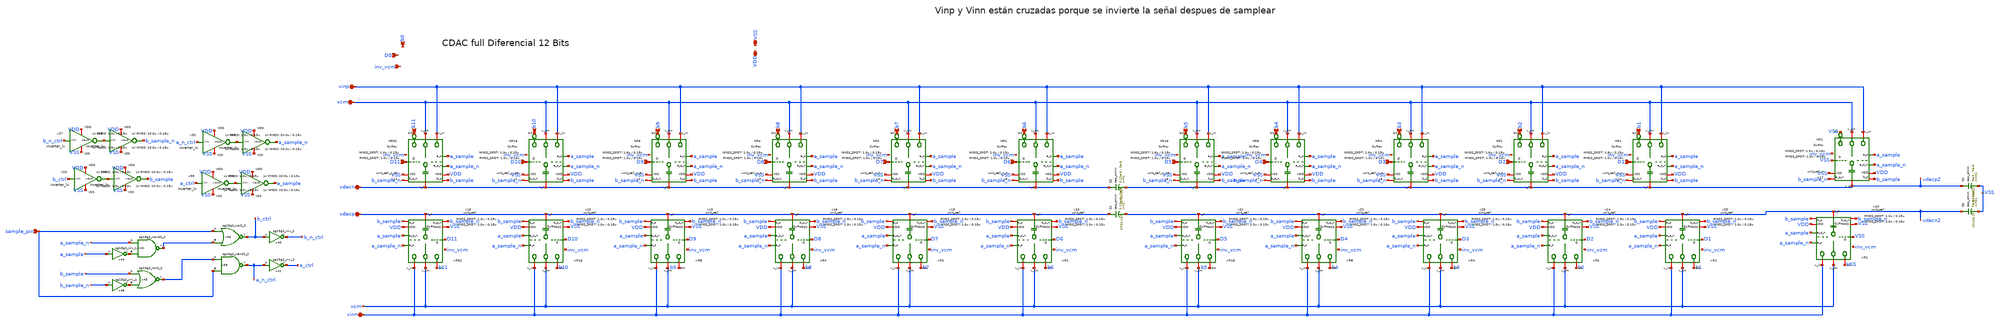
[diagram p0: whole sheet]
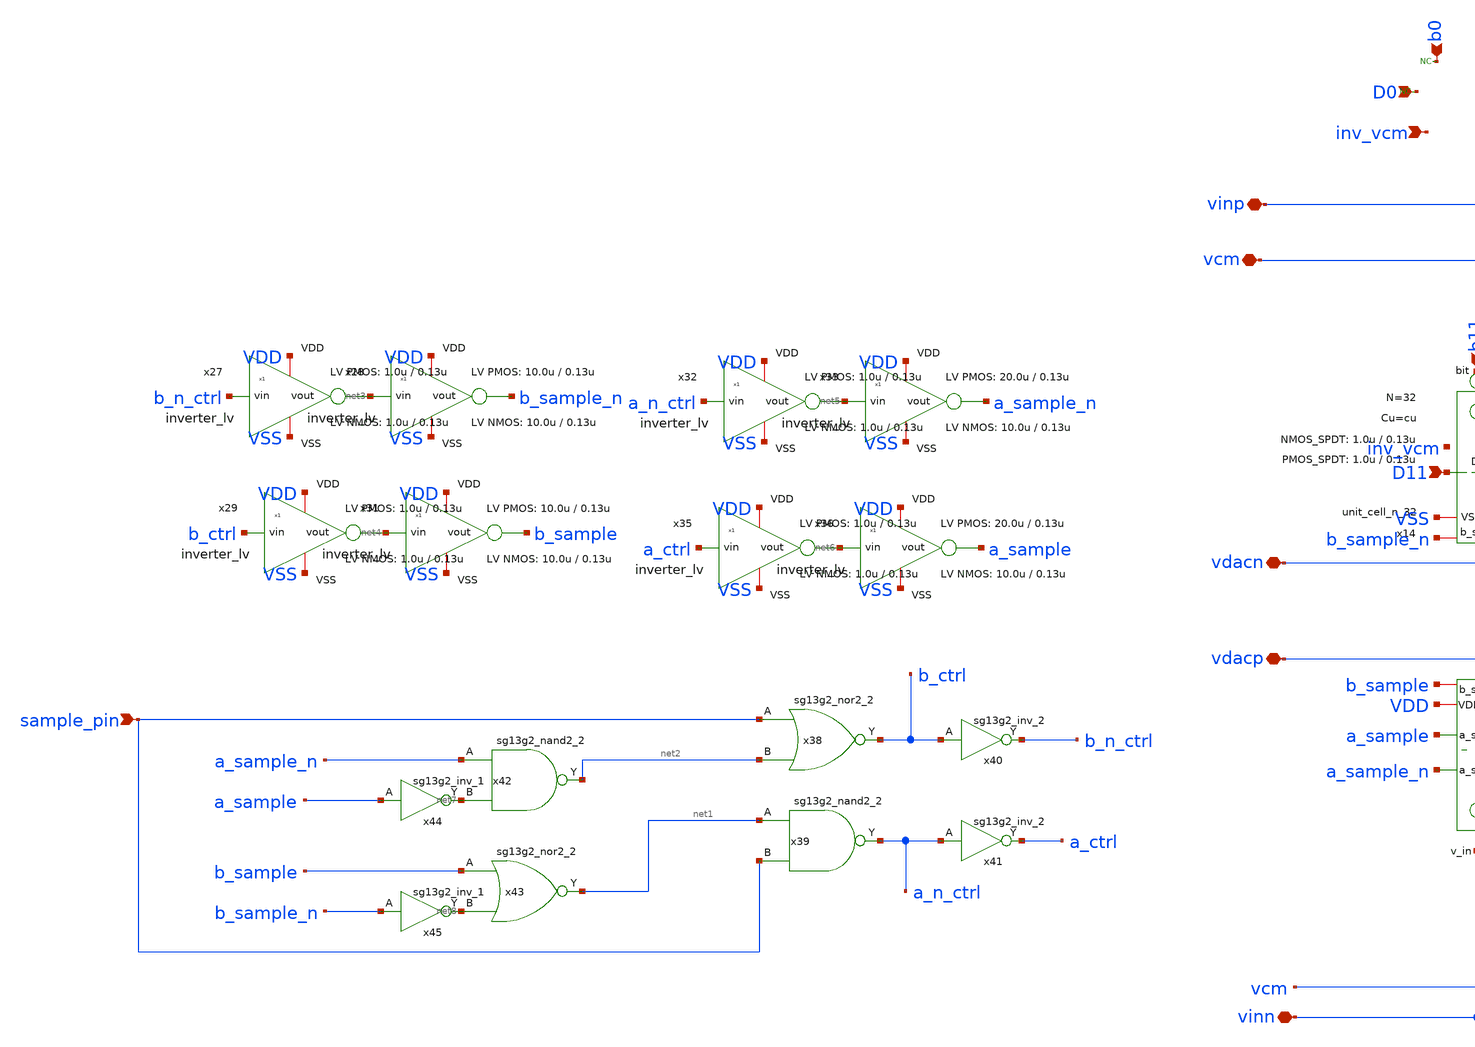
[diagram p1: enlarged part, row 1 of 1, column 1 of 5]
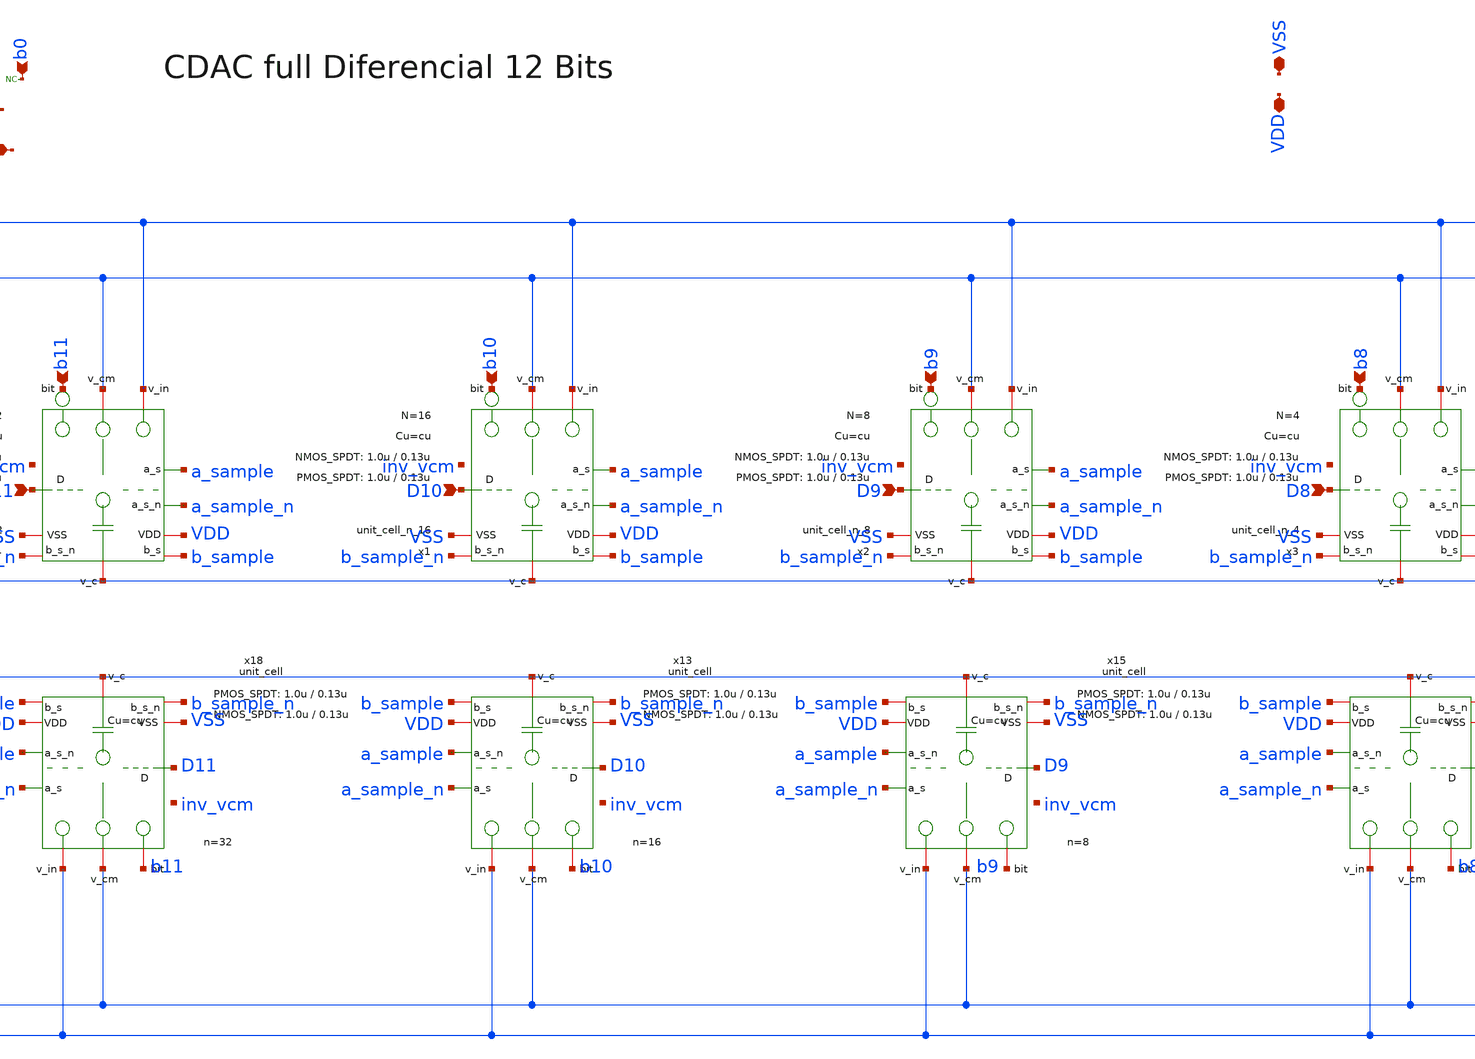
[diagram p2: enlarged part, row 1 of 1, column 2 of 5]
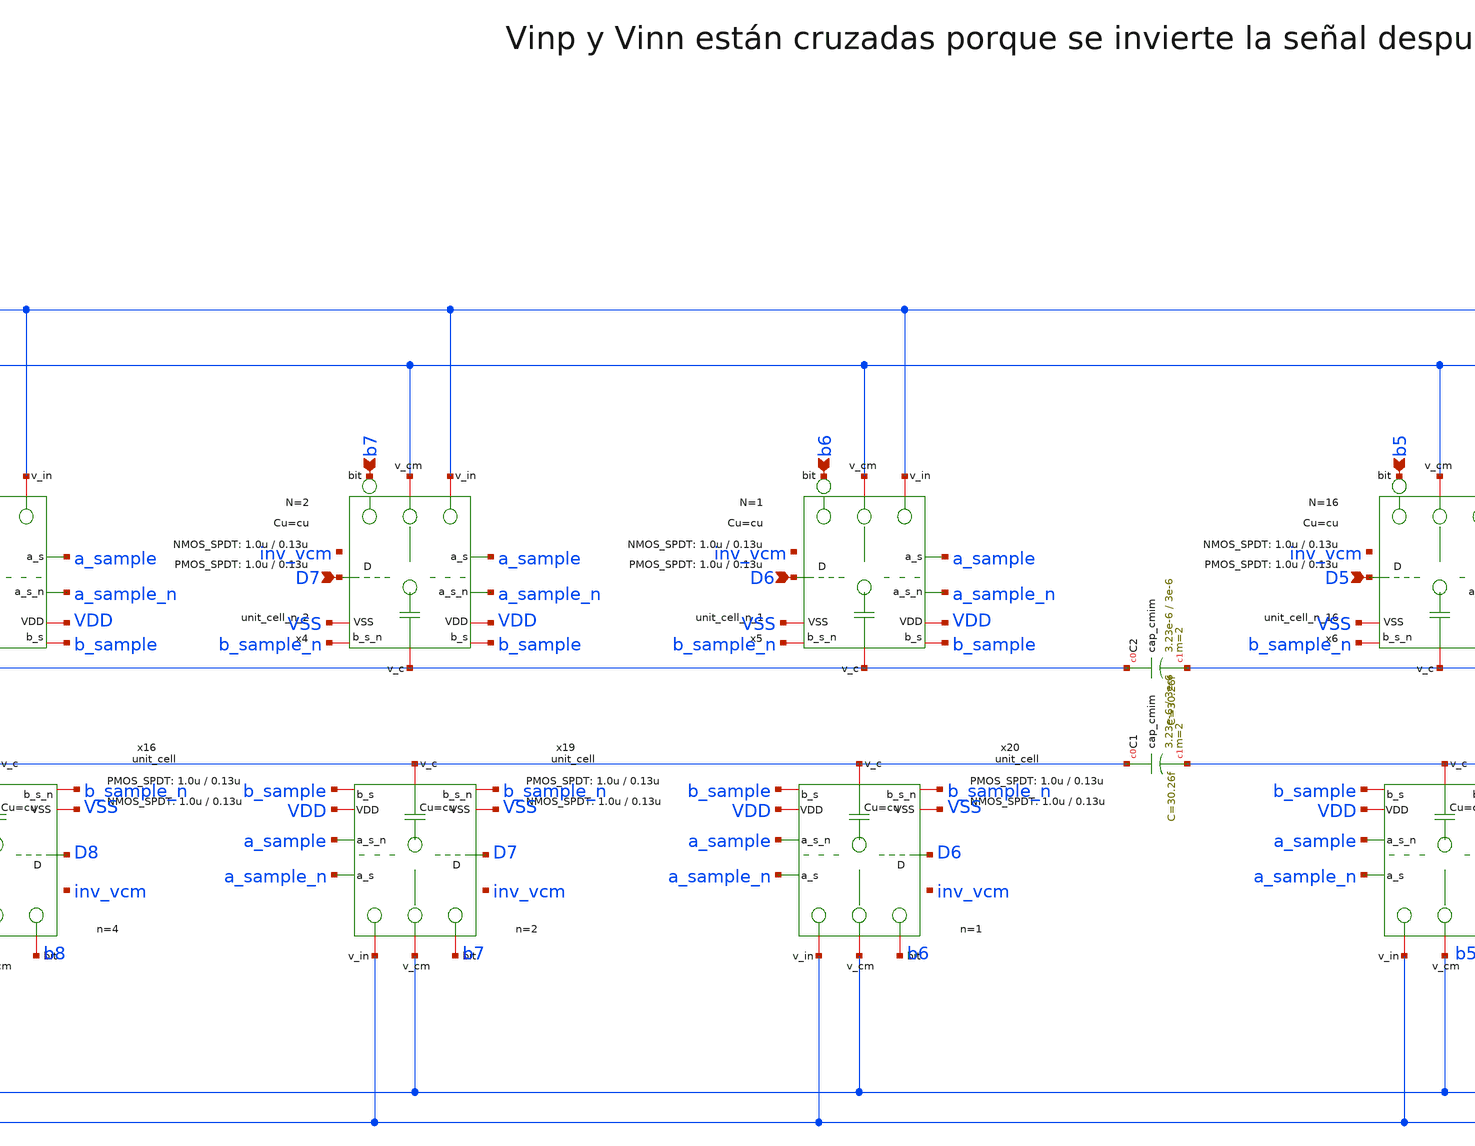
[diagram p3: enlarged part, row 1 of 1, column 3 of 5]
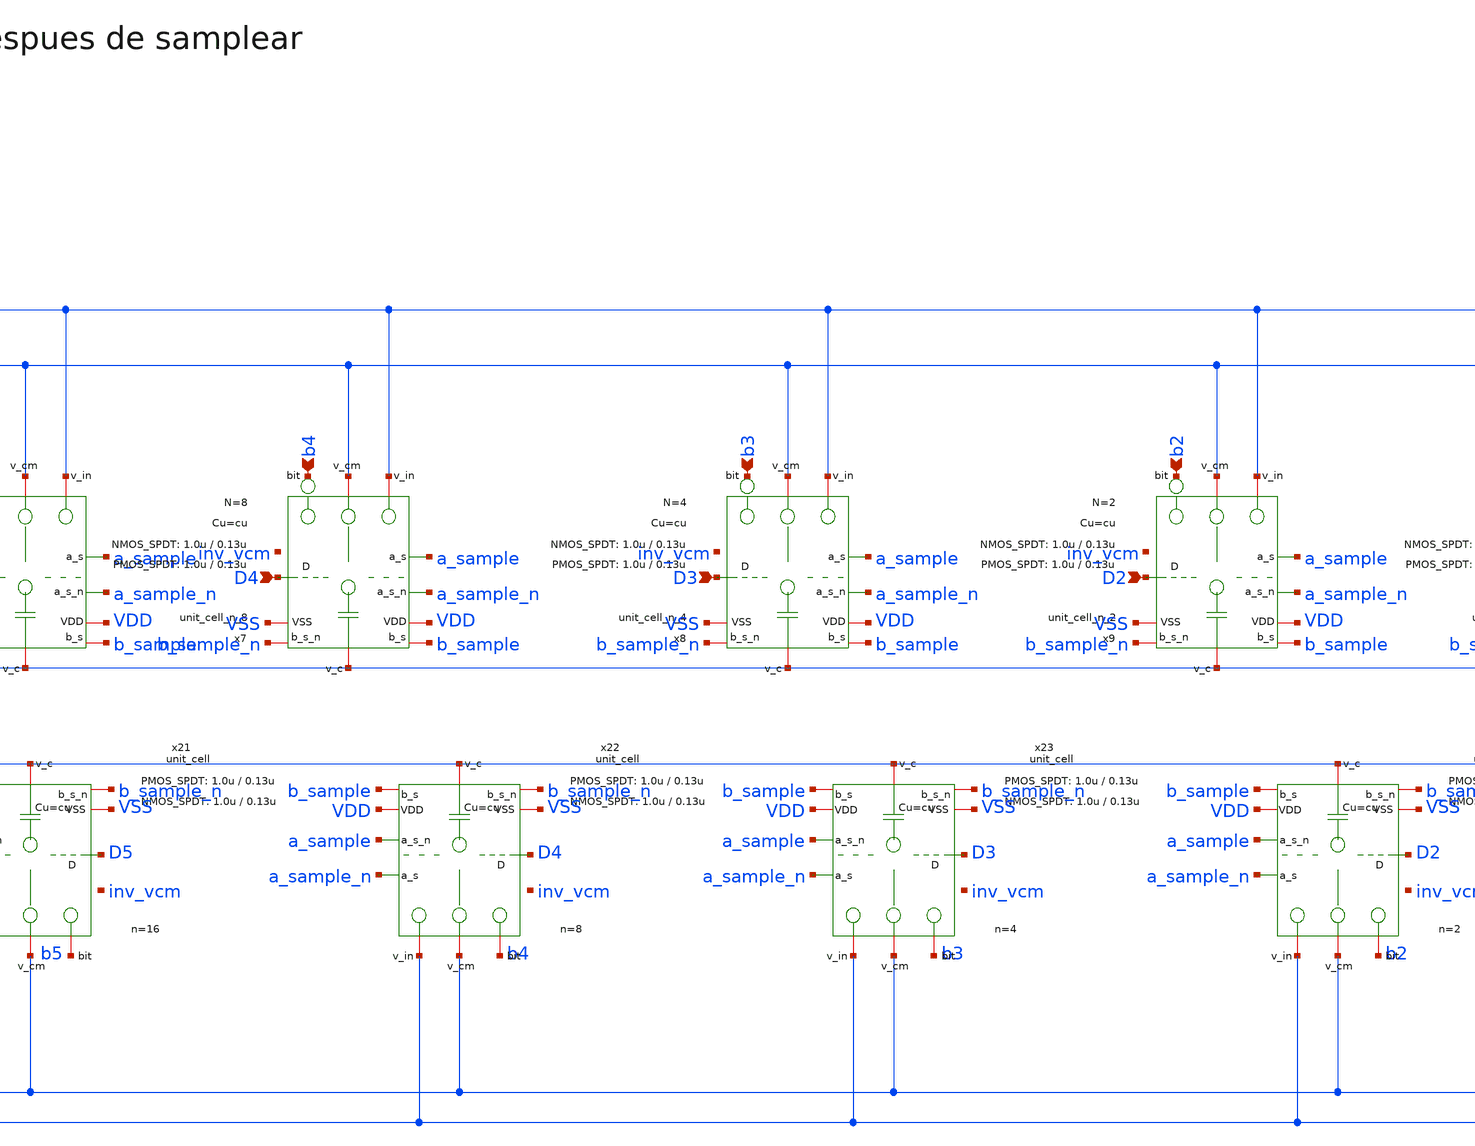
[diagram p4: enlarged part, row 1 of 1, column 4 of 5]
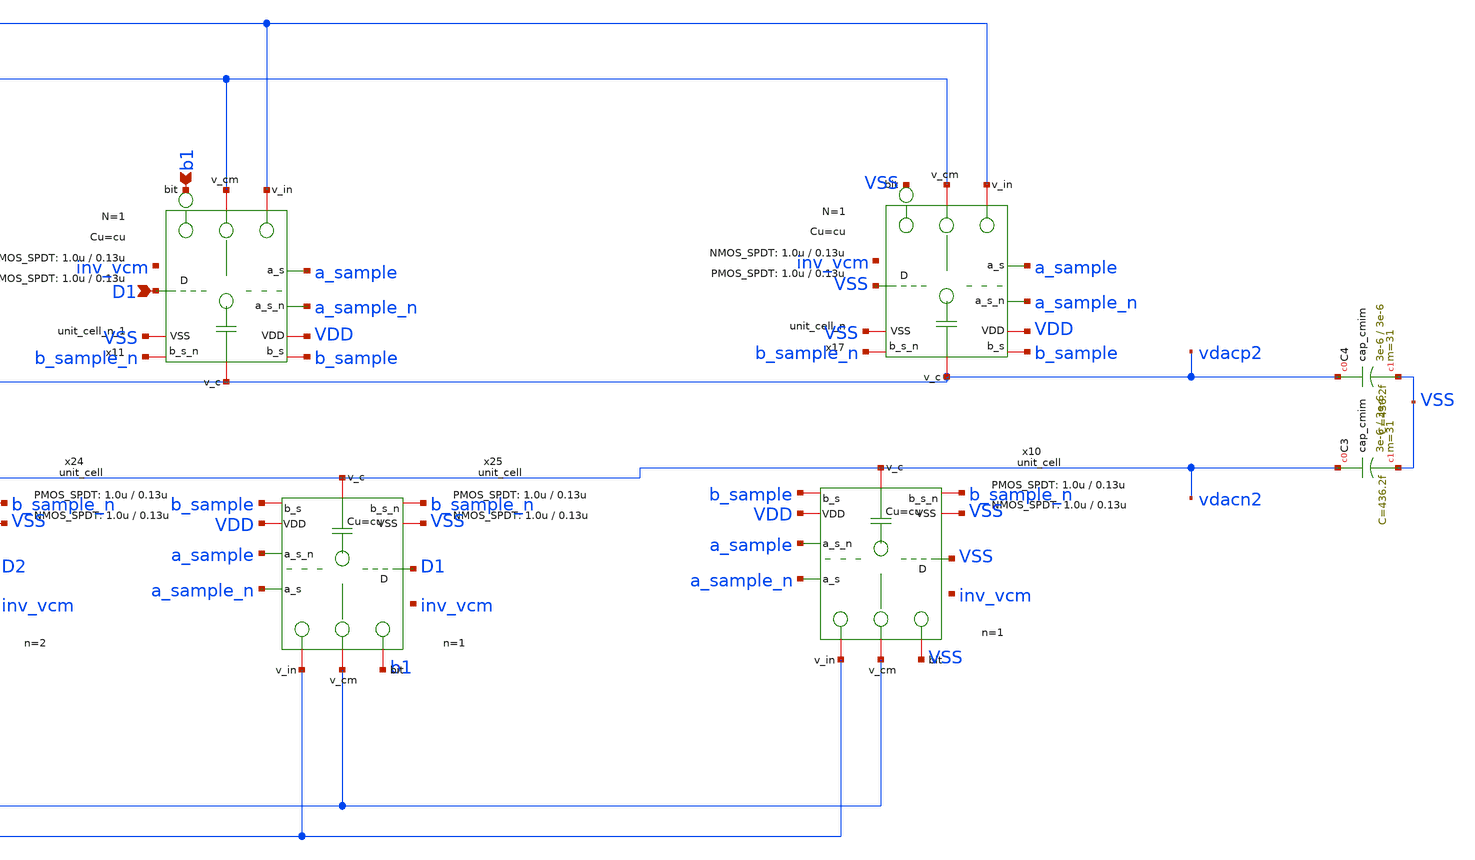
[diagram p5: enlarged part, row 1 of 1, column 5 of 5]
** sch_path: xschem/dac_icms_cell/dac.sch
**.subckt dac D0 b0 vinn vcm sample_pin vinp vdacp vdacn VSS VDD D1 b1 D2 b2 D3 b3 D4 b4 D5 b5 b6 D7
*+ b7 D8 b8 D9 b9 D10 b10 D11 b11 D6 inv_vcm
*.ipin D0
*.ipin b0
*.iopin vinn
*.iopin vcm
*.ipin sample_pin
*.iopin vinp
*.iopin vdacp
*.iopin vdacn
*.iopin VSS
*.iopin VDD
*.ipin D1
*.ipin b1
*.ipin D2
*.ipin b2
*.ipin D3
*.ipin b3
*.ipin D4
*.ipin b4
*.ipin D5
*.ipin b5
*.ipin b6
*.ipin D7
*.ipin b7
*.ipin D8
*.ipin b8
*.ipin D9
*.ipin b9
*.ipin D10
*.ipin b10
*.ipin D11
*.ipin b11
*.ipin D6
*.ipin inv_vcm
x14 VDD D11 VSS vdacn b11 vcm vinp a_sample a_sample_n b_sample b_sample_n inv_vcm unit_cell_n_32
x18 VDD D11 VSS vdacp b11 vcm vinn a_sample_n a_sample b_sample b_sample_n inv_vcm unit_cell W_P=
+ L_P_SPDT=0.13u W_N= L_N_SPDT=0.13u Cu=cu n=32
x1 VDD D10 VSS vdacn b10 vcm vinp a_sample a_sample_n b_sample b_sample_n inv_vcm unit_cell_n_16
x2 VDD D9 VSS vdacn b9 vcm vinp a_sample a_sample_n b_sample b_sample_n inv_vcm unit_cell_n_8
x3 VDD D8 VSS vdacn b8 vcm vinp a_sample a_sample_n b_sample b_sample_n inv_vcm unit_cell_n_4
x4 VDD D7 VSS vdacn b7 vcm vinp a_sample a_sample_n b_sample b_sample_n inv_vcm unit_cell_n_2
x5 VDD D6 VSS vdacn b6 vcm vinp a_sample a_sample_n b_sample b_sample_n inv_vcm unit_cell_n_1
x6 VDD D5 VSS vdacp2 b5 vcm vinp a_sample a_sample_n b_sample b_sample_n inv_vcm unit_cell_n_16
x7 VDD D4 VSS vdacp2 b4 vcm vinp a_sample a_sample_n b_sample b_sample_n inv_vcm unit_cell_n_8
x8 VDD D3 VSS vdacp2 b3 vcm vinp a_sample a_sample_n b_sample b_sample_n inv_vcm unit_cell_n_4
x9 VDD D2 VSS vdacp2 b2 vcm vinp a_sample a_sample_n b_sample b_sample_n inv_vcm unit_cell_n_2
x11 VDD D1 VSS vdacp2 b1 vcm vinp a_sample a_sample_n b_sample b_sample_n inv_vcm unit_cell_n_1
x13 VDD D10 VSS vdacp b10 vcm vinn a_sample_n a_sample b_sample b_sample_n inv_vcm unit_cell W_P=
+ L_P_SPDT=0.13u W_N= L_N_SPDT=0.13u Cu=cu n=16
x15 VDD D9 VSS vdacp b9 vcm vinn a_sample_n a_sample b_sample b_sample_n inv_vcm unit_cell W_P=
+ L_P_SPDT=0.13u W_N= L_N_SPDT=0.13u Cu=cu n=8
x16 VDD D8 VSS vdacp b8 vcm vinn a_sample_n a_sample b_sample b_sample_n inv_vcm unit_cell W_P=
+ L_P_SPDT=0.13u W_N= L_N_SPDT=0.13u Cu=cu n=4
x19 VDD D7 VSS vdacp b7 vcm vinn a_sample_n a_sample b_sample b_sample_n inv_vcm unit_cell W_P=1.0u
+ L_P_SPDT=0.13u W_N=1.0u L_N_SPDT=0.13u Cu=cu n=2
x20 VDD D6 VSS vdacp b6 vcm vinn a_sample_n a_sample b_sample b_sample_n inv_vcm unit_cell W_P=
+ L_P_SPDT=0.13u W_N= L_N_SPDT=0.13u Cu=cu n=1
x21 VDD D5 VSS vdacn2 b5 vcm vinn a_sample_n a_sample b_sample b_sample_n inv_vcm unit_cell W_P=
+ L_P_SPDT=0.13u W_N= L_N_SPDT=0.13u Cu=cu n=16
x22 VDD D4 VSS vdacn2 b4 vcm vinn a_sample_n a_sample b_sample b_sample_n inv_vcm unit_cell W_P=
+ L_P_SPDT=0.13u W_N= L_N_SPDT=0.13u Cu=cu n=8
x23 VDD D3 VSS vdacn2 b3 vcm vinn a_sample_n a_sample b_sample b_sample_n inv_vcm unit_cell W_P=
+ L_P_SPDT=0.13u W_N= L_N_SPDT=0.13u Cu=cu n=4
x24 VDD D2 VSS vdacn2 b2 vcm vinn a_sample_n a_sample b_sample b_sample_n inv_vcm unit_cell W_P=
+ L_P_SPDT=0.13u W_N= L_N_SPDT=0.13u Cu=cu n=2
x25 VDD D1 VSS vdacn2 b1 vcm vinn a_sample_n a_sample b_sample b_sample_n inv_vcm unit_cell W_P=
+ L_P_SPDT=0.13u W_N= L_N_SPDT=0.13u Cu=cu n=1
x27 VDD b_n_ctrl net3 VSS inverter_lv W_P=1.0u L_P=0.13u W_N=1.0u L_N=0.13u N_C=1
x28 VDD net3 b_sample_n VSS inverter_lv W_P=10.0u L_P=0.13u W_N=10.0u L_N=0.13u N_C=1
x29 VDD b_ctrl net4 VSS inverter_lv W_P=1.0u L_P=0.13u W_N=1.0u L_N=0.13u N_C=1
x31 VDD net4 b_sample VSS inverter_lv W_P=10.0u L_P=0.13u W_N=10.0u L_N=0.13u N_C=1
x32 VDD a_n_ctrl net5 VSS inverter_lv W_P=1.0u L_P=0.13u W_N=1.0u L_N=0.13u N_C=1
x33 VDD net5 a_sample_n VSS inverter_lv W_P=20.0u L_P=0.13u W_N=10.0u L_N=0.13u N_C=1
x35 VDD a_ctrl net6 VSS inverter_lv W_P=1.0u L_P=0.13u W_N=1.0u L_N=0.13u N_C=1
x36 VDD net6 a_sample VSS inverter_lv W_P=20.0u L_P=0.13u W_N=10.0u L_N=0.13u N_C=1
x38 b_ctrl sample_pin net2 VDD VSS sg13g2_nor2_2
x39 a_n_ctrl net1 sample_pin VDD VSS sg13g2_nand2_2
x40 b_n_ctrl b_ctrl VDD VSS sg13g2_inv_2
x41 a_ctrl a_n_ctrl VDD VSS sg13g2_inv_2
x42 net2 a_sample_n net7 VDD VSS sg13g2_nand2_2
x43 net1 b_sample net8 VDD VSS sg13g2_nor2_2
x44 net7 a_sample VDD VSS sg13g2_inv_1
x45 net8 b_sample_n VDD VSS sg13g2_inv_1
XC1 vdacp vdacn2 cap_cmim w=3.23e-6 l=3e-6 m=2 mm_ok=1
XC2 vdacn vdacp2 cap_cmim w=3.23e-6 l=3e-6 m=2 mm_ok=1
x10 VDD VSS VSS vdacn2 VSS vcm vinn a_sample_n a_sample b_sample b_sample_n inv_vcm unit_cell W_P=
+ L_P_SPDT=0.13u W_N= L_N_SPDT=0.13u Cu=cu n=1
x17 VDD VSS VSS vdacp2 VSS vcm vinp a_sample a_sample_n b_sample b_sample_n inv_vcm unit_cell_n
XC3 vdacn2 VSS cap_cmim w=3e-6 l=3e-6 m=31 mm_ok=1
XC4 vdacp2 VSS cap_cmim w=3e-6 l=3e-6 m=31 mm_ok=1
* noconn b0
* noconn D0
**.ends
.end
